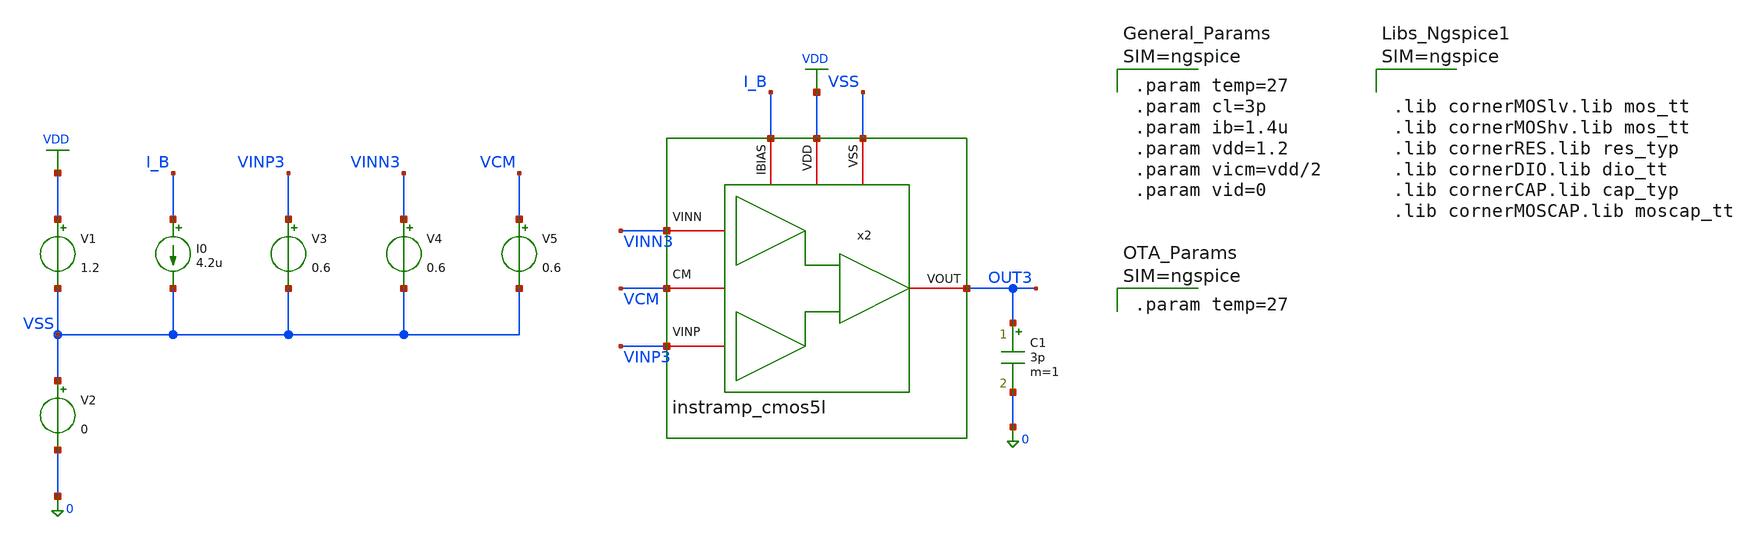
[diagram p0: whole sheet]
** sch_path: xschem/instramp_cmos5l/tb/tb_instramp_cmos5l_psrr/tb_instramp_cmos5l_psrr.sch
**.subckt tb_instramp_cmos5l_psrr
C1 OUT3 0 3p m=1
I0 I_B VSS 4.2u
V1 VDD VSS 1.2
V2 VSS 0 0
V3 VINP3 VSS 0.6
x2 VSS VDD I_B VINN3 OUT3 VINP3 VCM instramp_cmos5l
V4 VINN3 VSS 0.6
V5 VCM VSS 0.6
**** begin user architecture code



.lib cornerMOSlv.lib mos_tt
.lib cornerMOShv.lib mos_tt
.lib cornerRES.lib res_typ
.lib cornerDIO.lib dio_tt
.lib cornerCAP.lib cap_typ
.lib cornerMOSCAP.lib moscap_tt





.param temp=27
.param cl=3p
.param ib=1.4u
.param vdd=1.2
.param vicm=vdd/2
.param vid=0





.param temp=27





.control
save all
shell mkdir -p result

* PSRR (input-referred) = Adm / A_vdd,  A_vdd = v(out)/ripple on VDD
alter @v5[acmag]=0

* Run 1: differential gain (V3 = +0.5, V4 = -0.5 -> Vid = 1), supply quiet
alter @v1[acmag]=0
alter @v3[acmag]=0.5
alter @v3[acphase]=0
alter @v4[acmag]=0.5
alter @v4[acphase]=180
ac dec 20 1 10G
let vid = v(VINP3) - v(VINN3)
let adm = v(OUT3) / vid

* Run 2: 1 V ripple on VDD, inputs quiet
alter @v1[acmag]=1
alter @v3[acmag]=0
alter @v4[acmag]=0
ac dec 20 1 10G
let avdd = v(OUT3) / (v(VDD) - v(VSS))

let adm_db = db(ac1.adm)
let avdd_db = db(avdd)
let psrr_curve = db(ac1.adm / (avdd + 1e-15))

meas ac adm_dc find adm_db at=10
meas ac psrr_dc find psrr_curve at=10
meas ac psrr_100k find psrr_curve at=100k
meas ac psrr_1meg find psrr_curve at=1MEG

write ./result/tb_instramp_cmos5l_psrr.raw adm_db avdd_db psrr_curve

echo "======================================================="
echo "  Adm  @ DC / 10 Hz        : " $&adm_dc    " dB"
echo "  PSRR @ DC / 10 Hz        : " $&psrr_dc   " dB (Target: > 60 dB)"
echo "  PSRR @ 100 kHz           : " $&psrr_100k " dB"
echo "  PSRR @ 1 MHz             : " $&psrr_1meg " dB"
echo "======================================================="

plot psrr_curve xlog
.endc


**** end user architecture code
**.ends

* expanding   symbol:
*+  /foss/designs/sg13cmos5l_spma_ip__instramp/xschem/instramp_cmos5l/instramp_cmos5l.sym # of pins=7
** sym_path: /foss/designs/sg13cmos5l_spma_ip__instramp/xschem/instramp_cmos5l/instramp_cmos5l.sym
** sch_path: /foss/designs/sg13cmos5l_spma_ip__instramp/xschem/instramp_cmos5l/instramp_cmos5l.sch
.subckt instramp_cmos5l VSS VDD IBIAS VINN VOUT VINP CM
*.iopin VDD
*.iopin IBIAS
*.iopin VSS
*.iopin CM
*.iopin VOUT
*.iopin VINN
*.iopin VINP
x1 VSS IBIAS VDD net3 VINP net4 ota_cmos5l
x2 VSS IBIAS VDD net1 VINN net2 ota_cmos5l
x3 VSS IBIAS VDD net5 net6 VOUT ota_cmos5l
XR1 net4 net6 VSS rhigh w=0.5e-6 l=2e-6 m=1 b=0 mm_ok=1
XR2 net2 net5 VSS rhigh w=0.5e-6 l=2e-6 m=1 b=0 mm_ok=1
XR3 net6 CM VSS rhigh w=0.5e-6 l=8*2.23e-6 m=1 b=0 mm_ok=1
XR4 net5 VOUT VSS rhigh w=0.5e-6 l=8*2.23e-6 m=1 b=0 mm_ok=1
XR7 net2 net1 VSS rhigh w=0.5e-6 l=2e-6 m=1 b=0 mm_ok=1
XR8 net4 net3 VSS rhigh w=0.5e-6 l=2e-6 m=1 b=0 mm_ok=1
.ends


* expanding   symbol:  /foss/designs/sg13cmos5l_spma_ip__instramp/xschem/ota_cmos5l/ota_cmos5l.sym #
*+ of pins=6
** sym_path: xschem/output_buffer/ota_cmos5l.sym
** sch_path: xschem/output_buffer/ota_cmos5l.sch
.subckt ota_cmos5l VSS IBIAS VDD VINN VINP VOUT
*.iopin IBIAS
*.iopin VDD
*.iopin VSS
*.iopin VOUT
*.iopin VINP
*.iopin VINN
XM6 IBIAS IBIAS VDD VDD sg13_lv_pmos w={wbias} l={lbias} ng=1 m={m6} mm_ok=1
XM7 net1 IBIAS VDD VDD sg13_lv_pmos w={wbias} l={lbias} ng=1 m={m7} mm_ok=1
XM8 VOUT IBIAS VDD VDD sg13_lv_pmos w={wbias} l={lbias} ng=1 m={m8} mm_ok=1
XM1 net2 VINN net1 VDD sg13_lv_pmos w={winpair} l={linpair} ng=1 m=1 mm_ok=1
XM2 net3 VINP net1 VDD sg13_lv_pmos w={winpair} l={linpair} ng=1 m=1 mm_ok=1
XM3 net2 net2 VSS VSS sg13_lv_nmos w={wload} l={lload} ng=1 m=1 mm_ok=1
XM4 net3 net2 VSS VSS sg13_lv_nmos w={wload} l={lload} ng=1 m=1 mm_ok=1
XM5 VOUT net3 VSS VSS sg13_lv_nmos w={wcs} l={lcs} ng=1 m=1 mm_ok=1
XR1 net3 net4 VSS rhigh w=0.5e-6 l=1.95e-6 m=1 b=0 mm_ok=1
.save v(vinp)
.save v(vinn)
.save v(vout)
XC2 VOUT net4 cap_cmomi w=15e-6 l=15e-6 mmin=1 mmax=4 feed=double subblock=0 m=5 mm_ok=1
**** begin user architecture code


.param temp=27
.param lbias=0.15u wbias=0.15u
.param m6=1 m7=4 m8=8
.param linpair=3u winpair=20u
.param lload=5u wload=10u
.param lcs=3u wcs=20u
.param Cc=2p



**** end user architecture code
XC1 VOUT net4 cap_cmomi w=15e-6 l=15e-6 mmin=1 mmax=4 feed=double subblock=0 m=4 mm_ok=1
.ends

.GLOBAL VDD
.end
